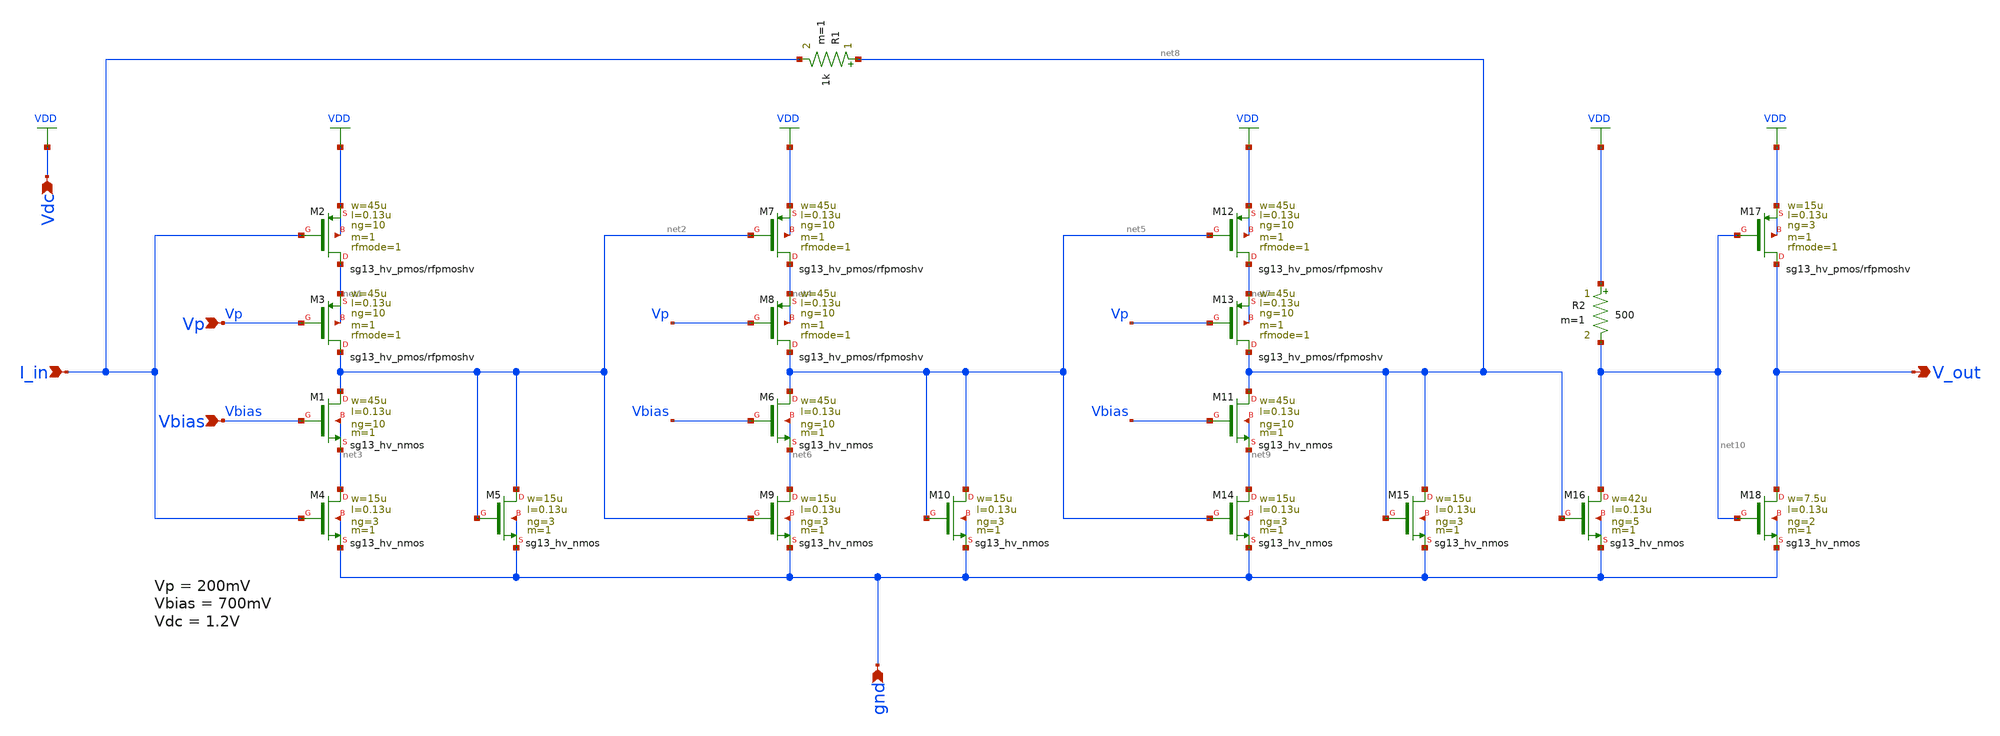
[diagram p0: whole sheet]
** sch_path: TIA_LSI/TIA_50GHz/design_data/xschem/schematic_50G_TIA.sch
* Copyright 2023 IHP PDK Authors
* Licensed under the Apache License, Version 2.0 (the "License");
* you may not use this file except in compliance with the License.
* You may obtain a copy of the License at
* https://www.apache.org/licenses/LICENSE-2.0
* Unless required by applicable law or agreed to in writing, software
* distributed under the License is distributed on an "AS IS" BASIS,
* WITHOUT WARRANTIES OR CONDITIONS OF ANY KIND, either express or implied.
* See the License for the specific language governing permissions and
* limitations under the License.
**.subckt schematic_50G_TIA Vp Vbias I_in gnd Vdc V_out
*.ipin Vp
*.ipin Vbias
*.ipin I_in
*.ipin gnd
*.ipin Vdc
*.opin V_out
XM1 net2 Vbias net3 net3 sg13_hv_nmos w=45u l=0.13u ng=10 m=1 mm_ok=1
XM2 net1 I_in VDD VDD sg13_hv_pmos w=45u l=0.13u ng=10 m=1 rfmode=1 mm_ok=1
R1 net8 I_in 1k m=1
XM3 net2 Vp net1 net1 sg13_hv_pmos w=45u l=0.13u ng=10 m=1 rfmode=1 mm_ok=1
XM4 net3 I_in gnd gnd sg13_hv_nmos w=15u l=0.13u ng=3 m=1 mm_ok=1
XM5 net2 net2 gnd gnd sg13_hv_nmos w=15u l=0.13u ng=3 m=1 mm_ok=1
XM6 net5 Vbias net6 net6 sg13_hv_nmos w=45u l=0.13u ng=10 m=1 mm_ok=1
XM7 net4 net2 VDD VDD sg13_hv_pmos w=45u l=0.13u ng=10 m=1 rfmode=1 mm_ok=1
XM8 net5 Vp net4 net4 sg13_hv_pmos w=45u l=0.13u ng=10 m=1 rfmode=1 mm_ok=1
XM9 net6 net2 gnd gnd sg13_hv_nmos w=15u l=0.13u ng=3 m=1 mm_ok=1
XM10 net5 net5 gnd gnd sg13_hv_nmos w=15u l=0.13u ng=3 m=1 mm_ok=1
XM11 net8 Vbias net9 net9 sg13_hv_nmos w=45u l=0.13u ng=10 m=1 mm_ok=1
XM12 net7 net5 VDD VDD sg13_hv_pmos w=45u l=0.13u ng=10 m=1 rfmode=1 mm_ok=1
XM13 net8 Vp net7 net7 sg13_hv_pmos w=45u l=0.13u ng=10 m=1 rfmode=1 mm_ok=1
XM14 net9 net5 gnd gnd sg13_hv_nmos w=15u l=0.13u ng=3 m=1 mm_ok=1
XM15 net8 net8 gnd gnd sg13_hv_nmos w=15u l=0.13u ng=3 m=1 mm_ok=1
R2 VDD net10 500 m=1
XM16 net10 net8 gnd gnd sg13_hv_nmos w=42u l=0.13u ng=5 m=1 mm_ok=1
XM17 V_out net10 VDD VDD sg13_hv_pmos w=15u l=0.13u ng=3 m=1 rfmode=1 mm_ok=1
XM18 V_out net10 gnd gnd sg13_hv_nmos w=7.5u l=0.13u ng=2 m=1 mm_ok=1
**.ends
.GLOBAL VDD
.end
